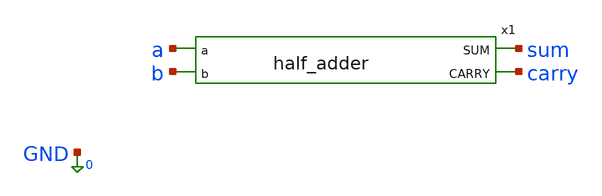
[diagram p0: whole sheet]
** sch_path: xschem_designs/half_adder_TB.sch
**.subckt half_adder_TB
x1 sum a b carry half_adder
**** begin user architecture code


.global VDD GND BP BN
.option temp=27
.include /usr/local/share/pdk/gf180mcuC/libs.tech/ngspice/design.ngspice
.lib /usr/local/share/pdk/gf180mcuC/libs.tech/ngspice/sm141064.ngspice typical

Vdd VDD 0 3.3
Vbp BP VDD 2.7
Vbn BN GND -2.7
Va a 0 PWL(0 0 89.9n 0 90.1n 1.4 179.9n 1.4 180.1n 3.3 269.9n 3.3 r=0)
Vb b 0 PWL(0 0 269.9n 0 270.1n 1.4 539.9n 1.4 540.1n 3.3  809.9n 3.3 r=0)

.control
  save all
  tran 0.1n 810n
  write half_adder_TB.raw
.endc
.end


**** end user architecture code
**.ends

* expanding   symbol:  xschem_designs/half_adder.sym # of pins=4
** sym_path: xschem_designs/half_adder.sym
** sch_path: xschem_designs/half_adder.sch
.subckt half_adder SUM a b CARRY
*.opin SUM
*.opin CARRY
*.ipin a
*.ipin b
XM1 NTI_a a GND GND nfet_03v3 L=0.28u W=0.22u nf=1 ad='int((nf+1)/2) * W/nf * 0.18u' as='int((nf+2)/2) * W/nf * 0.18u'
+ pd='2*int((nf+1)/2) * (W/nf + 0.18u)' ps='2*int((nf+2)/2) * (W/nf + 0.18u)' nrd='0.18u / W' nrs='0.18u / W'
+ sa=0 sb=0 sd=0 m=1 par=1
XM2 NTI_a a VDD BP pfet_06v0 L=1.1u W=0.60u nf=1 ad='int((nf+1)/2) * W/nf * 0.18u' as='int((nf+2)/2) * W/nf * 0.18u'
+ pd='2*int((nf+1)/2) * (W/nf + 0.18u)' ps='2*int((nf+2)/2) * (W/nf + 0.18u)' nrd='0.18u / W' nrs='0.18u / W'
+ sa=0 sb=0 sd=0 m=1 par=1
XM3 PTI_a a GND BN nfet_06v0 L=1.4u W=0.30u nf=1 ad='int((nf+1)/2) * W/nf * 0.18u' as='int((nf+2)/2) * W/nf * 0.18u'
+ pd='2*int((nf+1)/2) * (W/nf + 0.18u)' ps='2*int((nf+2)/2) * (W/nf + 0.18u)' nrd='0.18u / W' nrs='0.18u / W'
+ sa=0 sb=0 sd=0 m=1 par=1
XM7 amh a GND BN nfet_06v0 L=1.4u W=0.30u nf=1 ad='int((nf+1)/2) * W/nf * 0.18u' as='int((nf+2)/2) * W/nf * 0.18u'
+ pd='2*int((nf+1)/2) * (W/nf + 0.18u)' ps='2*int((nf+2)/2) * (W/nf + 0.18u)' nrd='0.18u / W' nrs='0.18u / W'
+ sa=0 sb=0 sd=0 m=1 par=1
XM8 amh NTI_a GND GND nfet_03v3 L=0.28u W=0.22u nf=1 ad='int((nf+1)/2) * W/nf * 0.18u' as='int((nf+2)/2) * W/nf * 0.18u'
+ pd='2*int((nf+1)/2) * (W/nf + 0.18u)' ps='2*int((nf+2)/2) * (W/nf + 0.18u)' nrd='0.18u / W' nrs='0.18u / W'
+ sa=0 sb=0 sd=0 m=1 par=1
XM9 NTI_b b GND GND nfet_03v3 L=0.28u W=0.22u nf=1 ad='int((nf+1)/2) * W/nf * 0.18u' as='int((nf+2)/2) * W/nf * 0.18u'
+ pd='2*int((nf+1)/2) * (W/nf + 0.18u)' ps='2*int((nf+2)/2) * (W/nf + 0.18u)' nrd='0.18u / W' nrs='0.18u / W'
+ sa=0 sb=0 sd=0 m=1 par=1
XM10 NTI_b b VDD BP pfet_06v0 L=1.1u W=0.60u nf=1 ad='int((nf+1)/2) * W/nf * 0.18u' as='int((nf+2)/2) * W/nf * 0.18u'
+ pd='2*int((nf+1)/2) * (W/nf + 0.18u)' ps='2*int((nf+2)/2) * (W/nf + 0.18u)' nrd='0.18u / W' nrs='0.18u / W'
+ sa=0 sb=0 sd=0 m=1 par=1
XM11 PTI_b b GND BN nfet_06v0 L=1.4u W=0.30u nf=1 ad='int((nf+1)/2) * W/nf * 0.18u' as='int((nf+2)/2) * W/nf * 0.18u'
+ pd='2*int((nf+1)/2) * (W/nf + 0.18u)' ps='2*int((nf+2)/2) * (W/nf + 0.18u)' nrd='0.18u / W' nrs='0.18u / W'
+ sa=0 sb=0 sd=0 m=1 par=1
XM15 bmh b GND BN nfet_06v0 L=1.4u W=0.30u nf=1 ad='int((nf+1)/2) * W/nf * 0.18u' as='int((nf+2)/2) * W/nf * 0.18u'
+ pd='2*int((nf+1)/2) * (W/nf + 0.18u)' ps='2*int((nf+2)/2) * (W/nf + 0.18u)' nrd='0.18u / W' nrs='0.18u / W'
+ sa=0 sb=0 sd=0 m=1 par=1
XM16 bmh NTI_b GND GND nfet_03v3 L=0.28u W=0.22u nf=1 ad='int((nf+1)/2) * W/nf * 0.18u' as='int((nf+2)/2) * W/nf * 0.18u'
+ pd='2*int((nf+1)/2) * (W/nf + 0.18u)' ps='2*int((nf+2)/2) * (W/nf + 0.18u)' nrd='0.18u / W' nrs='0.18u / W'
+ sa=0 sb=0 sd=0 m=1 par=1
XM17 net7 NTI_b GND GND nfet_03v3 L=0.28u W=0.22u nf=1 ad='int((nf+1)/2) * W/nf * 0.18u' as='int((nf+2)/2) * W/nf * 0.18u'
+ pd='2*int((nf+1)/2) * (W/nf + 0.18u)' ps='2*int((nf+2)/2) * (W/nf + 0.18u)' nrd='0.18u / W' nrs='0.18u / W'
+ sa=0 sb=0 sd=0 m=1 par=1
XM18 SUM NTI_a net7 GND nfet_03v3 L=0.28u W=0.22u nf=1 ad='int((nf+1)/2) * W/nf * 0.18u' as='int((nf+2)/2) * W/nf * 0.18u'
+ pd='2*int((nf+1)/2) * (W/nf + 0.18u)' ps='2*int((nf+2)/2) * (W/nf + 0.18u)' nrd='0.18u / W' nrs='0.18u / W'
+ sa=0 sb=0 sd=0 m=1 par=1
XM19 SUM amh net8 GND nfet_03v3 L=0.28u W=0.22u nf=1 ad='int((nf+1)/2) * W/nf * 0.18u' as='int((nf+2)/2) * W/nf * 0.18u'
+ pd='2*int((nf+1)/2) * (W/nf + 0.18u)' ps='2*int((nf+2)/2) * (W/nf + 0.18u)' nrd='0.18u / W' nrs='0.18u / W'
+ sa=0 sb=0 sd=0 m=1 par=1
XM20 net8 b GND BN nfet_06v0 L=1.4u W=0.30u nf=1 ad='int((nf+1)/2) * W/nf * 0.18u' as='int((nf+2)/2) * W/nf * 0.18u'
+ pd='2*int((nf+1)/2) * (W/nf + 0.18u)' ps='2*int((nf+2)/2) * (W/nf + 0.18u)' nrd='0.18u / W' nrs='0.18u / W'
+ sa=0 sb=0 sd=0 m=1 par=1
XM31 net9 a GND BN nfet_06v0 L=1.4u W=0.30u nf=1 ad='int((nf+1)/2) * W/nf * 0.18u' as='int((nf+2)/2) * W/nf * 0.18u'
+ pd='2*int((nf+1)/2) * (W/nf + 0.18u)' ps='2*int((nf+2)/2) * (W/nf + 0.18u)' nrd='0.18u / W' nrs='0.18u / W'
+ sa=0 sb=0 sd=0 m=1 par=1
XM32 SUM bmh net9 GND nfet_03v3 L=0.28u W=0.22u nf=1 ad='int((nf+1)/2) * W/nf * 0.18u' as='int((nf+2)/2) * W/nf * 0.18u'
+ pd='2*int((nf+1)/2) * (W/nf + 0.18u)' ps='2*int((nf+2)/2) * (W/nf + 0.18u)' nrd='0.18u / W' nrs='0.18u / W'
+ sa=0 sb=0 sd=0 m=1 par=1
XM33 aml amh GND GND nfet_03v3 L=0.28u W=0.22u nf=1 ad='int((nf+1)/2) * W/nf * 0.18u' as='int((nf+2)/2) * W/nf * 0.18u'
+ pd='2*int((nf+1)/2) * (W/nf + 0.18u)' ps='2*int((nf+2)/2) * (W/nf + 0.18u)' nrd='0.18u / W' nrs='0.18u / W'
+ sa=0 sb=0 sd=0 m=1 par=1
XM35 bml bmh GND GND nfet_03v3 L=0.28u W=0.22u nf=1 ad='int((nf+1)/2) * W/nf * 0.18u' as='int((nf+2)/2) * W/nf * 0.18u'
+ pd='2*int((nf+1)/2) * (W/nf + 0.18u)' ps='2*int((nf+2)/2) * (W/nf + 0.18u)' nrd='0.18u / W' nrs='0.18u / W'
+ sa=0 sb=0 sd=0 m=1 par=1
XM37 SUM a net10 BP pfet_06v0 L=1.1u W=0.60u nf=1 ad='int((nf+1)/2) * W/nf * 0.18u' as='int((nf+2)/2) * W/nf * 0.18u'
+ pd='2*int((nf+1)/2) * (W/nf + 0.18u)' ps='2*int((nf+2)/2) * (W/nf + 0.18u)' nrd='0.18u / W' nrs='0.18u / W'
+ sa=0 sb=0 sd=0 m=1 par=1
XM41 net11 b VDD BP pfet_06v0 L=1.1u W=0.60u nf=1 ad='int((nf+1)/2) * W/nf * 0.18u' as='int((nf+2)/2) * W/nf * 0.18u'
+ pd='2*int((nf+1)/2) * (W/nf + 0.18u)' ps='2*int((nf+2)/2) * (W/nf + 0.18u)' nrd='0.18u / W' nrs='0.18u / W'
+ sa=0 sb=0 sd=0 m=1 par=1
XM43 SUM SUM net2 GND nfet_03v3 L=2.24u W=0.22u nf=1 ad='int((nf+1)/2) * W/nf * 0.18u' as='int((nf+2)/2) * W/nf * 0.18u'
+ pd='2*int((nf+1)/2) * (W/nf + 0.18u)' ps='2*int((nf+2)/2) * (W/nf + 0.18u)' nrd='0.18u / W' nrs='0.18u / W'
+ sa=0 sb=0 sd=0 m=1 par=1
XM44 SUM SUM net1 VDD pfet_03v3 L=2.24u W=0.44u nf=1 ad='int((nf+1)/2) * W/nf * 0.18u' as='int((nf+2)/2) * W/nf * 0.18u'
+ pd='2*int((nf+1)/2) * (W/nf + 0.18u)' ps='2*int((nf+2)/2) * (W/nf + 0.18u)' nrd='0.18u / W' nrs='0.18u / W'
+ sa=0 sb=0 sd=0 m=1 par=1
XM51 net1 a net12 BP pfet_06v0 L=1.1u W=0.60u nf=1 ad='int((nf+1)/2) * W/nf * 0.18u' as='int((nf+2)/2) * W/nf * 0.18u'
+ pd='2*int((nf+1)/2) * (W/nf + 0.18u)' ps='2*int((nf+2)/2) * (W/nf + 0.18u)' nrd='0.18u / W' nrs='0.18u / W'
+ sa=0 sb=0 sd=0 m=1 par=1
XM57 net13 bmh GND GND nfet_03v3 L=0.28u W=0.22u nf=1 ad='int((nf+1)/2) * W/nf * 0.18u' as='int((nf+2)/2) * W/nf * 0.18u'
+ pd='2*int((nf+1)/2) * (W/nf + 0.18u)' ps='2*int((nf+2)/2) * (W/nf + 0.18u)' nrd='0.18u / W' nrs='0.18u / W'
+ sa=0 sb=0 sd=0 m=1 par=1
XM58 net2 NTI_a net13 GND nfet_03v3 L=0.28u W=0.22u nf=1 ad='int((nf+1)/2) * W/nf * 0.18u' as='int((nf+2)/2) * W/nf * 0.18u'
+ pd='2*int((nf+1)/2) * (W/nf + 0.18u)' ps='2*int((nf+2)/2) * (W/nf + 0.18u)' nrd='0.18u / W' nrs='0.18u / W'
+ sa=0 sb=0 sd=0 m=1 par=1
XM59 net2 amh net14 GND nfet_03v3 L=0.28u W=0.22u nf=1 ad='int((nf+1)/2) * W/nf * 0.18u' as='int((nf+2)/2) * W/nf * 0.18u'
+ pd='2*int((nf+1)/2) * (W/nf + 0.18u)' ps='2*int((nf+2)/2) * (W/nf + 0.18u)' nrd='0.18u / W' nrs='0.18u / W'
+ sa=0 sb=0 sd=0 m=1 par=1
XM61 net15 a GND BN nfet_06v0 L=1.4u W=0.30u nf=1 ad='int((nf+1)/2) * W/nf * 0.18u' as='int((nf+2)/2) * W/nf * 0.18u'
+ pd='2*int((nf+1)/2) * (W/nf + 0.18u)' ps='2*int((nf+2)/2) * (W/nf + 0.18u)' nrd='0.18u / W' nrs='0.18u / W'
+ sa=0 sb=0 sd=0 m=1 par=1
XM45 net14 NTI_b GND GND nfet_03v3 L=0.28u W=0.22u nf=1 ad='int((nf+1)/2) * W/nf * 0.18u' as='int((nf+2)/2) * W/nf * 0.18u'
+ pd='2*int((nf+1)/2) * (W/nf + 0.18u)' ps='2*int((nf+2)/2) * (W/nf + 0.18u)' nrd='0.18u / W' nrs='0.18u / W'
+ sa=0 sb=0 sd=0 m=1 par=1
XM46 net2 b net15 BN nfet_06v0 L=1.4u W=0.30u nf=1 ad='int((nf+1)/2) * W/nf * 0.18u' as='int((nf+2)/2) * W/nf * 0.18u'
+ pd='2*int((nf+1)/2) * (W/nf + 0.18u)' ps='2*int((nf+2)/2) * (W/nf + 0.18u)' nrd='0.18u / W' nrs='0.18u / W'
+ sa=0 sb=0 sd=0 m=1 par=1
XM47 net1 b net16 BP pfet_06v0 L=1.1u W=0.60u nf=1 ad='int((nf+1)/2) * W/nf * 0.18u' as='int((nf+2)/2) * W/nf * 0.18u'
+ pd='2*int((nf+1)/2) * (W/nf + 0.18u)' ps='2*int((nf+2)/2) * (W/nf + 0.18u)' nrd='0.18u / W' nrs='0.18u / W'
+ sa=0 sb=0 sd=0 m=1 par=1
XM237 net12 bml VDD VDD pfet_03v3 L=0.28u W=0.44u nf=1 ad='int((nf+1)/2) * W/nf * 0.18u' as='int((nf+2)/2) * W/nf * 0.18u'
+ pd='2*int((nf+1)/2) * (W/nf + 0.18u)' ps='2*int((nf+2)/2) * (W/nf + 0.18u)' nrd='0.18u / W' nrs='0.18u / W'
+ sa=0 sb=0 sd=0 m=1 par=1
XM4 PTI_b b VDD VDD pfet_03v3 L=0.28u W=0.44u nf=1 ad='int((nf+1)/2) * W/nf * 0.18u' as='int((nf+2)/2) * W/nf * 0.18u'
+ pd='2*int((nf+1)/2) * (W/nf + 0.18u)' ps='2*int((nf+2)/2) * (W/nf + 0.18u)' nrd='0.18u / W' nrs='0.18u / W'
+ sa=0 sb=0 sd=0 m=1 par=1
XM5 PTI_a a VDD VDD pfet_03v3 L=0.28u W=0.44u nf=1 ad='int((nf+1)/2) * W/nf * 0.18u' as='int((nf+2)/2) * W/nf * 0.18u'
+ pd='2*int((nf+1)/2) * (W/nf + 0.18u)' ps='2*int((nf+2)/2) * (W/nf + 0.18u)' nrd='0.18u / W' nrs='0.18u / W'
+ sa=0 sb=0 sd=0 m=1 par=1
XM6 net17 a VDD VDD pfet_03v3 L=0.28u W=0.44u nf=1 ad='int((nf+1)/2) * W/nf * 0.18u' as='int((nf+2)/2) * W/nf * 0.18u'
+ pd='2*int((nf+1)/2) * (W/nf + 0.18u)' ps='2*int((nf+2)/2) * (W/nf + 0.18u)' nrd='0.18u / W' nrs='0.18u / W'
+ sa=0 sb=0 sd=0 m=1 par=1
XM12 amh NTI_a net17 VDD pfet_03v3 L=0.28u W=0.44u nf=1 ad='int((nf+1)/2) * W/nf * 0.18u' as='int((nf+2)/2) * W/nf * 0.18u'
+ pd='2*int((nf+1)/2) * (W/nf + 0.18u)' ps='2*int((nf+2)/2) * (W/nf + 0.18u)' nrd='0.18u / W' nrs='0.18u / W'
+ sa=0 sb=0 sd=0 m=1 par=1
XM13 net18 b VDD VDD pfet_03v3 L=0.28u W=0.44u nf=1 ad='int((nf+1)/2) * W/nf * 0.18u' as='int((nf+2)/2) * W/nf * 0.18u'
+ pd='2*int((nf+1)/2) * (W/nf + 0.18u)' ps='2*int((nf+2)/2) * (W/nf + 0.18u)' nrd='0.18u / W' nrs='0.18u / W'
+ sa=0 sb=0 sd=0 m=1 par=1
XM14 bmh NTI_b net18 VDD pfet_03v3 L=0.28u W=0.44u nf=1 ad='int((nf+1)/2) * W/nf * 0.18u' as='int((nf+2)/2) * W/nf * 0.18u'
+ pd='2*int((nf+1)/2) * (W/nf + 0.18u)' ps='2*int((nf+2)/2) * (W/nf + 0.18u)' nrd='0.18u / W' nrs='0.18u / W'
+ sa=0 sb=0 sd=0 m=1 par=1
XM21 bml bmh VDD VDD pfet_03v3 L=0.28u W=0.44u nf=1 ad='int((nf+1)/2) * W/nf * 0.18u' as='int((nf+2)/2) * W/nf * 0.18u'
+ pd='2*int((nf+1)/2) * (W/nf + 0.18u)' ps='2*int((nf+2)/2) * (W/nf + 0.18u)' nrd='0.18u / W' nrs='0.18u / W'
+ sa=0 sb=0 sd=0 m=1 par=1
XM22 aml amh VDD VDD pfet_03v3 L=0.28u W=0.44u nf=1 ad='int((nf+1)/2) * W/nf * 0.18u' as='int((nf+2)/2) * W/nf * 0.18u'
+ pd='2*int((nf+1)/2) * (W/nf + 0.18u)' ps='2*int((nf+2)/2) * (W/nf + 0.18u)' nrd='0.18u / W' nrs='0.18u / W'
+ sa=0 sb=0 sd=0 m=1 par=1
XM23 net16 aml VDD VDD pfet_03v3 L=0.28u W=0.44u nf=1 ad='int((nf+1)/2) * W/nf * 0.18u' as='int((nf+2)/2) * W/nf * 0.18u'
+ pd='2*int((nf+1)/2) * (W/nf + 0.18u)' ps='2*int((nf+2)/2) * (W/nf + 0.18u)' nrd='0.18u / W' nrs='0.18u / W'
+ sa=0 sb=0 sd=0 m=1 par=1
XM24 net19 PTI_b VDD VDD pfet_03v3 L=0.28u W=0.44u nf=1 ad='int((nf+1)/2) * W/nf * 0.18u' as='int((nf+2)/2) * W/nf * 0.18u'
+ pd='2*int((nf+1)/2) * (W/nf + 0.18u)' ps='2*int((nf+2)/2) * (W/nf + 0.18u)' nrd='0.18u / W' nrs='0.18u / W'
+ sa=0 sb=0 sd=0 m=1 par=1
XM25 net1 PTI_a net19 VDD pfet_03v3 L=0.28u W=0.44u nf=1 ad='int((nf+1)/2) * W/nf * 0.18u' as='int((nf+2)/2) * W/nf * 0.18u'
+ pd='2*int((nf+1)/2) * (W/nf + 0.18u)' ps='2*int((nf+2)/2) * (W/nf + 0.18u)' nrd='0.18u / W' nrs='0.18u / W'
+ sa=0 sb=0 sd=0 m=1 par=1
XM26 SUM PTI_a net11 VDD pfet_03v3 L=0.28u W=0.44u nf=1 ad='int((nf+1)/2) * W/nf * 0.18u' as='int((nf+2)/2) * W/nf * 0.18u'
+ pd='2*int((nf+1)/2) * (W/nf + 0.18u)' ps='2*int((nf+2)/2) * (W/nf + 0.18u)' nrd='0.18u / W' nrs='0.18u / W'
+ sa=0 sb=0 sd=0 m=1 par=1
XM27 net20 aml VDD VDD pfet_03v3 L=0.28u W=0.44u nf=1 ad='int((nf+1)/2) * W/nf * 0.18u' as='int((nf+2)/2) * W/nf * 0.18u'
+ pd='2*int((nf+1)/2) * (W/nf + 0.18u)' ps='2*int((nf+2)/2) * (W/nf + 0.18u)' nrd='0.18u / W' nrs='0.18u / W'
+ sa=0 sb=0 sd=0 m=1 par=1
XM28 SUM bml net20 VDD pfet_03v3 L=0.28u W=0.44u nf=1 ad='int((nf+1)/2) * W/nf * 0.18u' as='int((nf+2)/2) * W/nf * 0.18u'
+ pd='2*int((nf+1)/2) * (W/nf + 0.18u)' ps='2*int((nf+2)/2) * (W/nf + 0.18u)' nrd='0.18u / W' nrs='0.18u / W'
+ sa=0 sb=0 sd=0 m=1 par=1
XM29 net10 PTI_b VDD VDD pfet_03v3 L=0.28u W=0.44u nf=1 ad='int((nf+1)/2) * W/nf * 0.18u' as='int((nf+2)/2) * W/nf * 0.18u'
+ pd='2*int((nf+1)/2) * (W/nf + 0.18u)' ps='2*int((nf+2)/2) * (W/nf + 0.18u)' nrd='0.18u / W' nrs='0.18u / W'
+ sa=0 sb=0 sd=0 m=1 par=1
XM30 net5 NTI_b GND GND nfet_03v3 L=0.28u W=0.22u nf=1 ad='int((nf+1)/2) * W/nf * 0.18u' as='int((nf+2)/2) * W/nf * 0.18u'
+ pd='2*int((nf+1)/2) * (W/nf + 0.18u)' ps='2*int((nf+2)/2) * (W/nf + 0.18u)' nrd='0.18u / W' nrs='0.18u / W'
+ sa=0 sb=0 sd=0 m=1 par=1
XM36 CARRY NTI_a net5 GND nfet_03v3 L=0.28u W=0.22u nf=1 ad='int((nf+1)/2) * W/nf * 0.18u' as='int((nf+2)/2) * W/nf * 0.18u'
+ pd='2*int((nf+1)/2) * (W/nf + 0.18u)' ps='2*int((nf+2)/2) * (W/nf + 0.18u)' nrd='0.18u / W' nrs='0.18u / W'
+ sa=0 sb=0 sd=0 m=1 par=1
XM39 net5 b GND BN nfet_06v0 L=1.4u W=0.30u nf=1 ad='int((nf+1)/2) * W/nf * 0.18u' as='int((nf+2)/2) * W/nf * 0.18u'
+ pd='2*int((nf+1)/2) * (W/nf + 0.18u)' ps='2*int((nf+2)/2) * (W/nf + 0.18u)' nrd='0.18u / W' nrs='0.18u / W'
+ sa=0 sb=0 sd=0 m=1 par=1
XM50 CARRY CARRY net3 VDD pfet_03v3 L=2.24u W=0.44u nf=1 ad='int((nf+1)/2) * W/nf * 0.18u' as='int((nf+2)/2) * W/nf * 0.18u'
+ pd='2*int((nf+1)/2) * (W/nf + 0.18u)' ps='2*int((nf+2)/2) * (W/nf + 0.18u)' nrd='0.18u / W' nrs='0.18u / W'
+ sa=0 sb=0 sd=0 m=1 par=1
XM54 net4 amh net21 GND nfet_03v3 L=0.28u W=0.22u nf=1 ad='int((nf+1)/2) * W/nf * 0.18u' as='int((nf+2)/2) * W/nf * 0.18u'
+ pd='2*int((nf+1)/2) * (W/nf + 0.18u)' ps='2*int((nf+2)/2) * (W/nf + 0.18u)' nrd='0.18u / W' nrs='0.18u / W'
+ sa=0 sb=0 sd=0 m=1 par=1
XM56 net22 a GND BN nfet_06v0 L=1.4u W=0.30u nf=1 ad='int((nf+1)/2) * W/nf * 0.18u' as='int((nf+2)/2) * W/nf * 0.18u'
+ pd='2*int((nf+1)/2) * (W/nf + 0.18u)' ps='2*int((nf+2)/2) * (W/nf + 0.18u)' nrd='0.18u / W' nrs='0.18u / W'
+ sa=0 sb=0 sd=0 m=1 par=1
XM60 net23 bmh GND GND nfet_03v3 L=0.28u W=0.22u nf=1 ad='int((nf+1)/2) * W/nf * 0.18u' as='int((nf+2)/2) * W/nf * 0.18u'
+ pd='2*int((nf+1)/2) * (W/nf + 0.18u)' ps='2*int((nf+2)/2) * (W/nf + 0.18u)' nrd='0.18u / W' nrs='0.18u / W'
+ sa=0 sb=0 sd=0 m=1 par=1
XM62 net4 b net22 BN nfet_06v0 L=1.4u W=0.30u nf=1 ad='int((nf+1)/2) * W/nf * 0.18u' as='int((nf+2)/2) * W/nf * 0.18u'
+ pd='2*int((nf+1)/2) * (W/nf + 0.18u)' ps='2*int((nf+2)/2) * (W/nf + 0.18u)' nrd='0.18u / W' nrs='0.18u / W'
+ sa=0 sb=0 sd=0 m=1 par=1
XM64 net24 aml VDD VDD pfet_03v3 L=0.28u W=0.44u nf=1 ad='int((nf+1)/2) * W/nf * 0.18u' as='int((nf+2)/2) * W/nf * 0.18u'
+ pd='2*int((nf+1)/2) * (W/nf + 0.18u)' ps='2*int((nf+2)/2) * (W/nf + 0.18u)' nrd='0.18u / W' nrs='0.18u / W'
+ sa=0 sb=0 sd=0 m=1 par=1
XM66 net25 PTI_b VDD VDD pfet_03v3 L=0.28u W=0.44u nf=1 ad='int((nf+1)/2) * W/nf * 0.18u' as='int((nf+2)/2) * W/nf * 0.18u'
+ pd='2*int((nf+1)/2) * (W/nf + 0.18u)' ps='2*int((nf+2)/2) * (W/nf + 0.18u)' nrd='0.18u / W' nrs='0.18u / W'
+ sa=0 sb=0 sd=0 m=1 par=1
XM67 net3 PTI_a net25 VDD pfet_03v3 L=0.28u W=0.44u nf=1 ad='int((nf+1)/2) * W/nf * 0.18u' as='int((nf+2)/2) * W/nf * 0.18u'
+ pd='2*int((nf+1)/2) * (W/nf + 0.18u)' ps='2*int((nf+2)/2) * (W/nf + 0.18u)' nrd='0.18u / W' nrs='0.18u / W'
+ sa=0 sb=0 sd=0 m=1 par=1
XM42 net21 b GND BN nfet_06v0 L=1.4u W=0.30u nf=1 ad='int((nf+1)/2) * W/nf * 0.18u' as='int((nf+2)/2) * W/nf * 0.18u'
+ pd='2*int((nf+1)/2) * (W/nf + 0.18u)' ps='2*int((nf+2)/2) * (W/nf + 0.18u)' nrd='0.18u / W' nrs='0.18u / W'
+ sa=0 sb=0 sd=0 m=1 par=1
XM48 net3 PTI_b net24 VDD pfet_03v3 L=0.28u W=0.44u nf=1 ad='int((nf+1)/2) * W/nf * 0.18u' as='int((nf+2)/2) * W/nf * 0.18u'
+ pd='2*int((nf+1)/2) * (W/nf + 0.18u)' ps='2*int((nf+2)/2) * (W/nf + 0.18u)' nrd='0.18u / W' nrs='0.18u / W'
+ sa=0 sb=0 sd=0 m=1 par=1
XM52 net4 a net23 BN nfet_06v0 L=1.4u W=0.30u nf=1 ad='int((nf+1)/2) * W/nf * 0.18u' as='int((nf+2)/2) * W/nf * 0.18u'
+ pd='2*int((nf+1)/2) * (W/nf + 0.18u)' ps='2*int((nf+2)/2) * (W/nf + 0.18u)' nrd='0.18u / W' nrs='0.18u / W'
+ sa=0 sb=0 sd=0 m=1 par=1
XM55 net3 bml net26 VDD pfet_03v3 L=0.28u W=0.44u nf=1 ad='int((nf+1)/2) * W/nf * 0.18u' as='int((nf+2)/2) * W/nf * 0.18u'
+ pd='2*int((nf+1)/2) * (W/nf + 0.18u)' ps='2*int((nf+2)/2) * (W/nf + 0.18u)' nrd='0.18u / W' nrs='0.18u / W'
+ sa=0 sb=0 sd=0 m=1 par=1
XM63 net6 NTI_b GND GND nfet_03v3 L=0.28u W=0.22u nf=1 ad='int((nf+1)/2) * W/nf * 0.18u' as='int((nf+2)/2) * W/nf * 0.18u'
+ pd='2*int((nf+1)/2) * (W/nf + 0.18u)' ps='2*int((nf+2)/2) * (W/nf + 0.18u)' nrd='0.18u / W' nrs='0.18u / W'
+ sa=0 sb=0 sd=0 m=1 par=1
XM68 CARRY amh net6 GND nfet_03v3 L=0.28u W=0.22u nf=1 ad='int((nf+1)/2) * W/nf * 0.18u' as='int((nf+2)/2) * W/nf * 0.18u'
+ pd='2*int((nf+1)/2) * (W/nf + 0.18u)' ps='2*int((nf+2)/2) * (W/nf + 0.18u)' nrd='0.18u / W' nrs='0.18u / W'
+ sa=0 sb=0 sd=0 m=1 par=1
XM38 net5 bmh GND GND nfet_03v3 L=0.28u W=0.22u nf=1 ad='int((nf+1)/2) * W/nf * 0.18u' as='int((nf+2)/2) * W/nf * 0.18u'
+ pd='2*int((nf+1)/2) * (W/nf + 0.18u)' ps='2*int((nf+2)/2) * (W/nf + 0.18u)' nrd='0.18u / W' nrs='0.18u / W'
+ sa=0 sb=0 sd=0 m=1 par=1
XM69 net6 bmh GND GND nfet_03v3 L=0.28u W=0.22u nf=1 ad='int((nf+1)/2) * W/nf * 0.18u' as='int((nf+2)/2) * W/nf * 0.18u'
+ pd='2*int((nf+1)/2) * (W/nf + 0.18u)' ps='2*int((nf+2)/2) * (W/nf + 0.18u)' nrd='0.18u / W' nrs='0.18u / W'
+ sa=0 sb=0 sd=0 m=1 par=1
XM70 net27 NTI_b GND GND nfet_03v3 L=0.28u W=0.22u nf=1 ad='int((nf+1)/2) * W/nf * 0.18u' as='int((nf+2)/2) * W/nf * 0.18u'
+ pd='2*int((nf+1)/2) * (W/nf + 0.18u)' ps='2*int((nf+2)/2) * (W/nf + 0.18u)' nrd='0.18u / W' nrs='0.18u / W'
+ sa=0 sb=0 sd=0 m=1 par=1
XM71 CARRY a net27 BN nfet_06v0 L=1.4u W=0.30u nf=1 ad='int((nf+1)/2) * W/nf * 0.18u' as='int((nf+2)/2) * W/nf * 0.18u'
+ pd='2*int((nf+1)/2) * (W/nf + 0.18u)' ps='2*int((nf+2)/2) * (W/nf + 0.18u)' nrd='0.18u / W' nrs='0.18u / W'
+ sa=0 sb=0 sd=0 m=1 par=1
XM34 net26 PTI_a VDD VDD pfet_03v3 L=0.28u W=0.44u nf=1 ad='int((nf+1)/2) * W/nf * 0.18u' as='int((nf+2)/2) * W/nf * 0.18u'
+ pd='2*int((nf+1)/2) * (W/nf + 0.18u)' ps='2*int((nf+2)/2) * (W/nf + 0.18u)' nrd='0.18u / W' nrs='0.18u / W'
+ sa=0 sb=0 sd=0 m=1 par=1
XM40 CARRY CARRY net4 GND nfet_03v3 L=2.24u W=0.22u nf=1 ad='int((nf+1)/2) * W/nf * 0.18u' as='int((nf+2)/2) * W/nf * 0.18u'
+ pd='2*int((nf+1)/2) * (W/nf + 0.18u)' ps='2*int((nf+2)/2) * (W/nf + 0.18u)' nrd='0.18u / W' nrs='0.18u / W'
+ sa=0 sb=0 sd=0 m=1 par=1
.ends

.end
